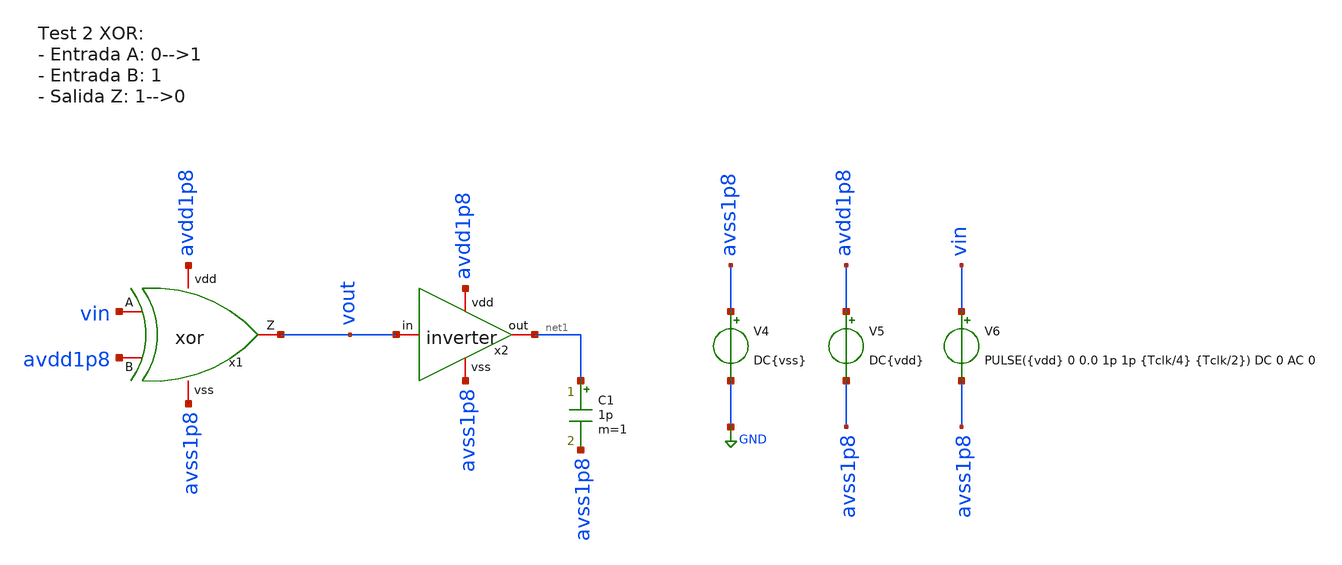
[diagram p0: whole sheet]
** sch_path: designs/sch/tests/test2_xor.sch
**.subckt test2_xor
x2 avdd1p8 net1 vout avss1p8 inverter
V4 avss1p8 GND DC{vss}
V5 avdd1p8 avss1p8 DC{vdd}
V6 vin avss1p8 PULSE({vdd} 0 0.0 1p 1p {Tclk/4} {Tclk/2}) DC 0 AC 0
C1 net1 avss1p8 1p m=1
x1 avdd1p8 vout vin avdd1p8 avss1p8 xor
**** begin user architecture code


* Circuit Parameters
.param vdd = 1.8
.param vss = 0.0
.param Tclk = 10n
.options TEMP = 65.0

* Include Models
.lib /foss/pdks/sky130A/libs.tech/ngspice/sky130.lib.spice TT

* OP Parameters & Singals to save
.save all

* Simulations
.control
  tran 0.01u 100n
  setplot tran1
  plot v(vin) v(vout)+2
reset
  dc V6 0 1.8 0.01
  setplot dc
  plot vin vout ylabel vout xlabel vin
  set filetype = ascii
  write dcsweep.raw
.endc

.end


**** end user architecture code
**.ends

* expanding   symbol:  /foss/designs/sch/inverter.sym # of pins=4
** sym_path: designs/inverter.sym
** sch_path: designs/inverter.sch
.subckt inverter vdd out in vss
*.iopin out
*.iopin vss
*.iopin vdd
*.iopin in
XM2 out in vss vss sky130_fd_pr__nfet_01v8 L=0.15 W=0.75 nf=1 ad='int((nf+1)/2) * W/nf * 0.29' as='int((nf+2)/2) * W/nf * 0.29'
+ pd='2*int((nf+1)/2) * (W/nf + 0.29)' ps='2*int((nf+2)/2) * (W/nf + 0.29)' nrd='0.29 / W' nrs='0.29 / W'
+ sa=0 sb=0 sd=0 mult=1 m=1
XM1 out in vdd vdd sky130_fd_pr__pfet_01v8 L=0.15 W=1.5 nf=1 ad='int((nf+1)/2) * W/nf * 0.29' as='int((nf+2)/2) * W/nf * 0.29'
+ pd='2*int((nf+1)/2) * (W/nf + 0.29)' ps='2*int((nf+2)/2) * (W/nf + 0.29)' nrd='0.29 / W' nrs='0.29 / W'
+ sa=0 sb=0 sd=0 mult=1 m=1
.ends


* expanding   symbol:  /foss/designs/sch/xor.sym # of pins=5
** sym_path: designs/xor.sym
** sch_path: designs/xor.sch
.subckt xor vdd Z A B vss
*.iopin A
*.iopin B
*.iopin vdd
*.iopin Z
*.iopin vss
XM6 net1 Bb vss vss sky130_fd_pr__nfet_01v8 L=0.15 W=1.5 nf=1 ad='int((nf+1)/2) * W/nf * 0.29' as='int((nf+2)/2) * W/nf * 0.29'
+ pd='2*int((nf+1)/2) * (W/nf + 0.29)' ps='2*int((nf+2)/2) * (W/nf + 0.29)' nrd='0.29 / W' nrs='0.29 / W'
+ sa=0 sb=0 sd=0 mult=1 m=1
XM4 Z Ab net1 vss sky130_fd_pr__nfet_01v8 L=0.15 W=1.5 nf=1 ad='int((nf+1)/2) * W/nf * 0.29' as='int((nf+2)/2) * W/nf * 0.29'
+ pd='2*int((nf+1)/2) * (W/nf + 0.29)' ps='2*int((nf+2)/2) * (W/nf + 0.29)' nrd='0.29 / W' nrs='0.29 / W'
+ sa=0 sb=0 sd=0 mult=1 m=1
XM5 Z A net2 vss sky130_fd_pr__nfet_01v8 L=0.15 W=1.5 nf=1 ad='int((nf+1)/2) * W/nf * 0.29' as='int((nf+2)/2) * W/nf * 0.29'
+ pd='2*int((nf+1)/2) * (W/nf + 0.29)' ps='2*int((nf+2)/2) * (W/nf + 0.29)' nrd='0.29 / W' nrs='0.29 / W'
+ sa=0 sb=0 sd=0 mult=1 m=1
XM7 net2 B vss vss sky130_fd_pr__nfet_01v8 L=0.15 W=1.5 nf=1 ad='int((nf+1)/2) * W/nf * 0.29' as='int((nf+2)/2) * W/nf * 0.29'
+ pd='2*int((nf+1)/2) * (W/nf + 0.29)' ps='2*int((nf+2)/2) * (W/nf + 0.29)' nrd='0.29 / W' nrs='0.29 / W'
+ sa=0 sb=0 sd=0 mult=1 m=1
XM0 net3 Bb vdd vdd sky130_fd_pr__pfet_01v8 L=0.15 W=1.5 nf=1 ad='int((nf+1)/2) * W/nf * 0.29' as='int((nf+2)/2) * W/nf * 0.29'
+ pd='2*int((nf+1)/2) * (W/nf + 0.29)' ps='2*int((nf+2)/2) * (W/nf + 0.29)' nrd='0.29 / W' nrs='0.29 / W'
+ sa=0 sb=0 sd=0 mult=1 m=1
XM1 net4 Ab vdd vdd sky130_fd_pr__pfet_01v8 L=0.15 W=1.5 nf=1 ad='int((nf+1)/2) * W/nf * 0.29' as='int((nf+2)/2) * W/nf * 0.29'
+ pd='2*int((nf+1)/2) * (W/nf + 0.29)' ps='2*int((nf+2)/2) * (W/nf + 0.29)' nrd='0.29 / W' nrs='0.29 / W'
+ sa=0 sb=0 sd=0 mult=1 m=1
XM2 Z A net3 vdd sky130_fd_pr__pfet_01v8 L=0.15 W=1.5 nf=1 ad='int((nf+1)/2) * W/nf * 0.29' as='int((nf+2)/2) * W/nf * 0.29'
+ pd='2*int((nf+1)/2) * (W/nf + 0.29)' ps='2*int((nf+2)/2) * (W/nf + 0.29)' nrd='0.29 / W' nrs='0.29 / W'
+ sa=0 sb=0 sd=0 mult=1 m=1
XM3 Z B net4 vdd sky130_fd_pr__pfet_01v8 L=0.15 W=1.5 nf=1 ad='int((nf+1)/2) * W/nf * 0.29' as='int((nf+2)/2) * W/nf * 0.29'
+ pd='2*int((nf+1)/2) * (W/nf + 0.29)' ps='2*int((nf+2)/2) * (W/nf + 0.29)' nrd='0.29 / W' nrs='0.29 / W'
+ sa=0 sb=0 sd=0 mult=1 m=1
x1 vdd Ab A vss inverter
x2 vdd Bb B vss inverter
.ends

.GLOBAL GND
.end
